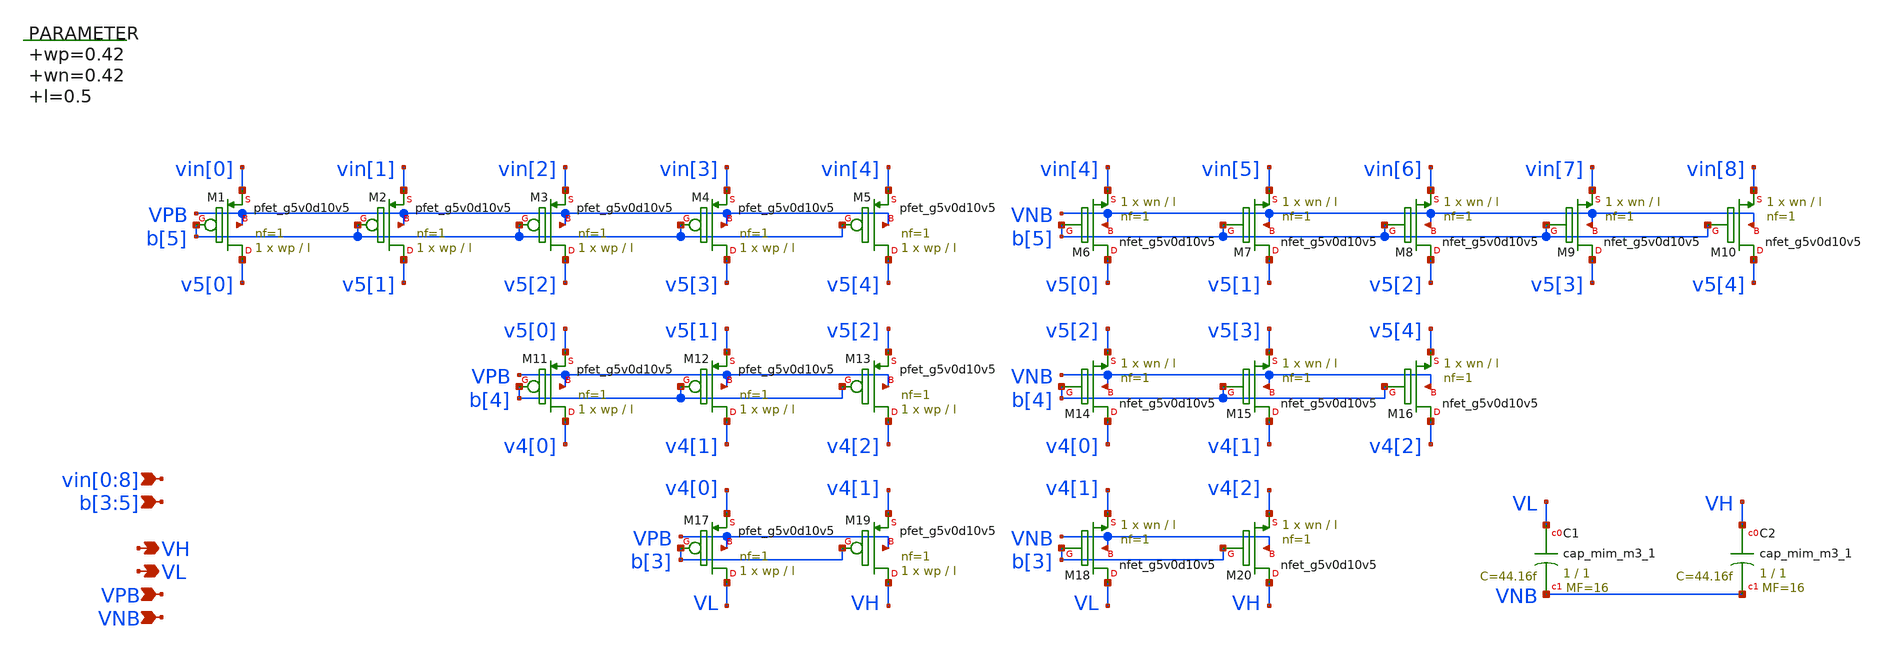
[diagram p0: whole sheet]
** sch_path: xschem/vselector_3b_2v.sch
**.subckt vselector_3b_2v vin[0],vin[1],vin[2],vin[3],vin[4],vin[5],vin[6],vin[7],vin[8] VH VPB VNB
*+ b[3],b[4],b[5] VL
*.ipin vin[0],vin[1],vin[2],vin[3],vin[4],vin[5],vin[6],vin[7],vin[8]
*.opin VH
*.ipin VPB
*.ipin VNB
*.ipin b[3],b[4],b[5]
*.opin VL
XM1 v5[0] b[5] vin[0] VPB sky130_fd_pr__pfet_g5v0d10v5 L=l W=wp nf=1 ad='int((nf+1)/2) * W/nf * 0.29'
+ as='int((nf+2)/2) * W/nf * 0.29' pd='2*int((nf+1)/2) * (W/nf + 0.29)' ps='2*int((nf+2)/2) * (W/nf + 0.29)'
+ nrd='0.29 / W' nrs='0.29 / W' sa=0 sb=0 sd=0 mult=1 m=1
XM6 v5[0] b[5] vin[4] VNB sky130_fd_pr__nfet_g5v0d10v5 L=l W=wn nf=1 ad='int((nf+1)/2) * W/nf * 0.29'
+ as='int((nf+2)/2) * W/nf * 0.29' pd='2*int((nf+1)/2) * (W/nf + 0.29)' ps='2*int((nf+2)/2) * (W/nf + 0.29)'
+ nrd='0.29 / W' nrs='0.29 / W' sa=0 sb=0 sd=0 mult=1 m=1
.param wp=0.42 wn=0.42 l=0.5

XM2 v5[1] b[5] vin[1] VPB sky130_fd_pr__pfet_g5v0d10v5 L=l W=wp nf=1 ad='int((nf+1)/2) * W/nf * 0.29'
+ as='int((nf+2)/2) * W/nf * 0.29' pd='2*int((nf+1)/2) * (W/nf + 0.29)' ps='2*int((nf+2)/2) * (W/nf + 0.29)'
+ nrd='0.29 / W' nrs='0.29 / W' sa=0 sb=0 sd=0 mult=1 m=1
XM3 v5[2] b[5] vin[2] VPB sky130_fd_pr__pfet_g5v0d10v5 L=l W=wp nf=1 ad='int((nf+1)/2) * W/nf * 0.29'
+ as='int((nf+2)/2) * W/nf * 0.29' pd='2*int((nf+1)/2) * (W/nf + 0.29)' ps='2*int((nf+2)/2) * (W/nf + 0.29)'
+ nrd='0.29 / W' nrs='0.29 / W' sa=0 sb=0 sd=0 mult=1 m=1
XM4 v5[3] b[5] vin[3] VPB sky130_fd_pr__pfet_g5v0d10v5 L=l W=wp nf=1 ad='int((nf+1)/2) * W/nf * 0.29'
+ as='int((nf+2)/2) * W/nf * 0.29' pd='2*int((nf+1)/2) * (W/nf + 0.29)' ps='2*int((nf+2)/2) * (W/nf + 0.29)'
+ nrd='0.29 / W' nrs='0.29 / W' sa=0 sb=0 sd=0 mult=1 m=1
XM5 v5[4] b[5] vin[4] VPB sky130_fd_pr__pfet_g5v0d10v5 L=l W=wp nf=1 ad='int((nf+1)/2) * W/nf * 0.29'
+ as='int((nf+2)/2) * W/nf * 0.29' pd='2*int((nf+1)/2) * (W/nf + 0.29)' ps='2*int((nf+2)/2) * (W/nf + 0.29)'
+ nrd='0.29 / W' nrs='0.29 / W' sa=0 sb=0 sd=0 mult=1 m=1
XM11 v4[0] b[4] v5[0] VPB sky130_fd_pr__pfet_g5v0d10v5 L=l W=wp nf=1 ad='int((nf+1)/2) * W/nf * 0.29'
+ as='int((nf+2)/2) * W/nf * 0.29' pd='2*int((nf+1)/2) * (W/nf + 0.29)' ps='2*int((nf+2)/2) * (W/nf + 0.29)'
+ nrd='0.29 / W' nrs='0.29 / W' sa=0 sb=0 sd=0 mult=1 m=1
XM12 v4[1] b[4] v5[1] VPB sky130_fd_pr__pfet_g5v0d10v5 L=l W=wp nf=1 ad='int((nf+1)/2) * W/nf * 0.29'
+ as='int((nf+2)/2) * W/nf * 0.29' pd='2*int((nf+1)/2) * (W/nf + 0.29)' ps='2*int((nf+2)/2) * (W/nf + 0.29)'
+ nrd='0.29 / W' nrs='0.29 / W' sa=0 sb=0 sd=0 mult=1 m=1
XM13 v4[2] b[4] v5[2] VPB sky130_fd_pr__pfet_g5v0d10v5 L=l W=wp nf=1 ad='int((nf+1)/2) * W/nf * 0.29'
+ as='int((nf+2)/2) * W/nf * 0.29' pd='2*int((nf+1)/2) * (W/nf + 0.29)' ps='2*int((nf+2)/2) * (W/nf + 0.29)'
+ nrd='0.29 / W' nrs='0.29 / W' sa=0 sb=0 sd=0 mult=1 m=1
XM17 VL b[3] v4[0] VPB sky130_fd_pr__pfet_g5v0d10v5 L=l W=wp nf=1 ad='int((nf+1)/2) * W/nf * 0.29' as='int((nf+2)/2) * W/nf * 0.29'
+ pd='2*int((nf+1)/2) * (W/nf + 0.29)' ps='2*int((nf+2)/2) * (W/nf + 0.29)' nrd='0.29 / W' nrs='0.29 / W'
+ sa=0 sb=0 sd=0 mult=1 m=1
XM19 VH b[3] v4[1] VPB sky130_fd_pr__pfet_g5v0d10v5 L=l W=wp nf=1 ad='int((nf+1)/2) * W/nf * 0.29' as='int((nf+2)/2) * W/nf * 0.29'
+ pd='2*int((nf+1)/2) * (W/nf + 0.29)' ps='2*int((nf+2)/2) * (W/nf + 0.29)' nrd='0.29 / W' nrs='0.29 / W'
+ sa=0 sb=0 sd=0 mult=1 m=1
XM7 v5[1] b[5] vin[5] VNB sky130_fd_pr__nfet_g5v0d10v5 L=l W=wn nf=1 ad='int((nf+1)/2) * W/nf * 0.29'
+ as='int((nf+2)/2) * W/nf * 0.29' pd='2*int((nf+1)/2) * (W/nf + 0.29)' ps='2*int((nf+2)/2) * (W/nf + 0.29)'
+ nrd='0.29 / W' nrs='0.29 / W' sa=0 sb=0 sd=0 mult=1 m=1
XM8 v5[2] b[5] vin[6] VNB sky130_fd_pr__nfet_g5v0d10v5 L=l W=wn nf=1 ad='int((nf+1)/2) * W/nf * 0.29'
+ as='int((nf+2)/2) * W/nf * 0.29' pd='2*int((nf+1)/2) * (W/nf + 0.29)' ps='2*int((nf+2)/2) * (W/nf + 0.29)'
+ nrd='0.29 / W' nrs='0.29 / W' sa=0 sb=0 sd=0 mult=1 m=1
XM9 v5[3] b[5] vin[7] VNB sky130_fd_pr__nfet_g5v0d10v5 L=l W=wn nf=1 ad='int((nf+1)/2) * W/nf * 0.29'
+ as='int((nf+2)/2) * W/nf * 0.29' pd='2*int((nf+1)/2) * (W/nf + 0.29)' ps='2*int((nf+2)/2) * (W/nf + 0.29)'
+ nrd='0.29 / W' nrs='0.29 / W' sa=0 sb=0 sd=0 mult=1 m=1
XM10 v5[4] b[5] vin[8] VNB sky130_fd_pr__nfet_g5v0d10v5 L=l W=wn nf=1 ad='int((nf+1)/2) * W/nf * 0.29'
+ as='int((nf+2)/2) * W/nf * 0.29' pd='2*int((nf+1)/2) * (W/nf + 0.29)' ps='2*int((nf+2)/2) * (W/nf + 0.29)'
+ nrd='0.29 / W' nrs='0.29 / W' sa=0 sb=0 sd=0 mult=1 m=1
XM14 v4[0] b[4] v5[2] VNB sky130_fd_pr__nfet_g5v0d10v5 L=l W=wn nf=1 ad='int((nf+1)/2) * W/nf * 0.29'
+ as='int((nf+2)/2) * W/nf * 0.29' pd='2*int((nf+1)/2) * (W/nf + 0.29)' ps='2*int((nf+2)/2) * (W/nf + 0.29)'
+ nrd='0.29 / W' nrs='0.29 / W' sa=0 sb=0 sd=0 mult=1 m=1
XM15 v4[1] b[4] v5[3] VNB sky130_fd_pr__nfet_g5v0d10v5 L=l W=wn nf=1 ad='int((nf+1)/2) * W/nf * 0.29'
+ as='int((nf+2)/2) * W/nf * 0.29' pd='2*int((nf+1)/2) * (W/nf + 0.29)' ps='2*int((nf+2)/2) * (W/nf + 0.29)'
+ nrd='0.29 / W' nrs='0.29 / W' sa=0 sb=0 sd=0 mult=1 m=1
XM16 v4[2] b[4] v5[4] VNB sky130_fd_pr__nfet_g5v0d10v5 L=l W=wn nf=1 ad='int((nf+1)/2) * W/nf * 0.29'
+ as='int((nf+2)/2) * W/nf * 0.29' pd='2*int((nf+1)/2) * (W/nf + 0.29)' ps='2*int((nf+2)/2) * (W/nf + 0.29)'
+ nrd='0.29 / W' nrs='0.29 / W' sa=0 sb=0 sd=0 mult=1 m=1
XM18 VL b[3] v4[1] VNB sky130_fd_pr__nfet_g5v0d10v5 L=l W=wn nf=1 ad='int((nf+1)/2) * W/nf * 0.29' as='int((nf+2)/2) * W/nf * 0.29'
+ pd='2*int((nf+1)/2) * (W/nf + 0.29)' ps='2*int((nf+2)/2) * (W/nf + 0.29)' nrd='0.29 / W' nrs='0.29 / W'
+ sa=0 sb=0 sd=0 mult=1 m=1
XM20 VH b[3] v4[2] VNB sky130_fd_pr__nfet_g5v0d10v5 L=l W=wn nf=1 ad='int((nf+1)/2) * W/nf * 0.29' as='int((nf+2)/2) * W/nf * 0.29'
+ pd='2*int((nf+1)/2) * (W/nf + 0.29)' ps='2*int((nf+2)/2) * (W/nf + 0.29)' nrd='0.29 / W' nrs='0.29 / W'
+ sa=0 sb=0 sd=0 mult=1 m=1
XC1 VL VNB sky130_fd_pr__cap_mim_m3_1 W=1 L=1 MF=16 m=16
XC2 VH VNB sky130_fd_pr__cap_mim_m3_1 W=1 L=1 MF=16 m=16
**.ends
.end
